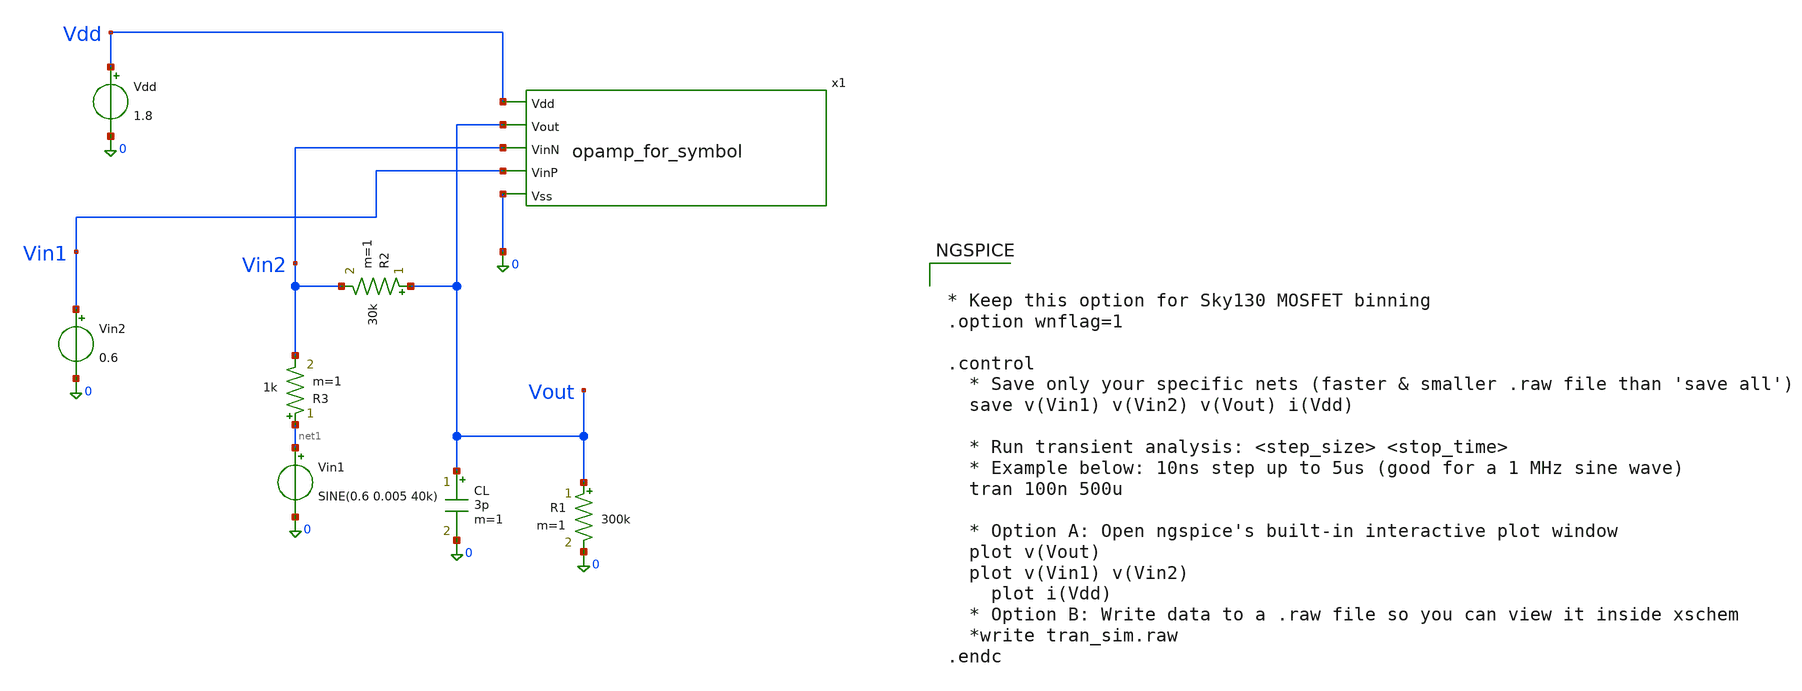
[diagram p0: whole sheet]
** sch_path: parameter_extraction/opamp_testbench.sch
**.subckt opamp_testbench
x1 Vdd Vout Vin2 Vin1 0 opamp_for_symbol
Vdd Vdd 0 1.8
Vin1 net1 0 SINE(0.6 0.005 40k)
Vin2 Vin1 0 0.6
CL Vout 0 3p m=1
R1 Vout 0 300k m=1
R2 Vout Vin2 30k m=1
R3 net1 Vin2 1k m=1
**** begin user architecture code

** opencircuitdesign pdks install
.lib $::SKYWATER_MODELS/sky130.lib.spice tt



* Keep this option for Sky130 MOSFET binning
.option wnflag=1

.control
  * Save only your specific nets (faster & smaller .raw file than 'save all')
  save v(Vin1) v(Vin2) v(Vout) i(Vdd)

  * Run transient analysis: <step_size> <stop_time>
  * Example below: 10ns step up to 5us (good for a 1 MHz sine wave)
  tran 100n 500u

  * Option A: Open ngspice's built-in interactive plot window
  plot v(Vout)
  plot v(Vin1) v(Vin2)
	plot i(Vdd)
  * Option B: Write data to a .raw file so you can view it inside xschem
  *write tran_sim.raw
.endc


**** end user architecture code
**.ends
.end
